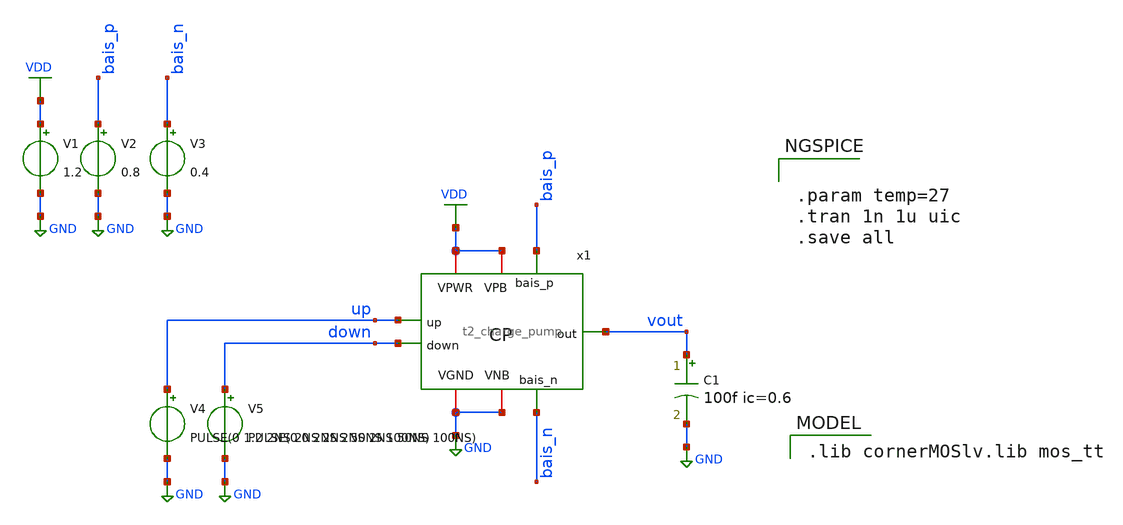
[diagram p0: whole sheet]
** sch_path: Team 2 Design/design_data/xschem/t2_charge_pump_tb.sch
**.subckt t2_charge_pump_tb
V1 VDD GND 1.2
V2 bais_p GND 0.8
V3 bais_n GND 0.4
V4 up GND PULSE(0 1.2 2NS 2NS 2NS 50NS 100NS)
V5 down GND PULSE(0 0 2NS 2NS 2NS 50NS 100NS)
C1 vout GND 100f ic=0.6 m=1
x1 VDD VDD GND GND vout up down bais_p bais_n t2_charge_pump
**** begin user architecture code


.param temp=27
.tran 1n 1u uic
.save all


 .lib cornerMOSlv.lib mos_tt

**** end user architecture code
**.ends
.GLOBAL GND
.GLOBAL VDD
.end
